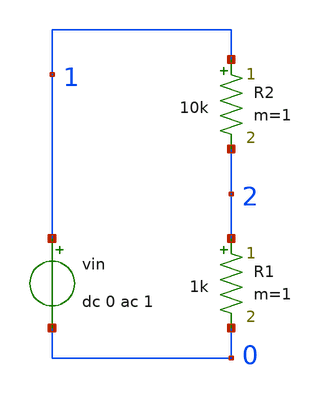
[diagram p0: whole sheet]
** sch_path: test_noise.sch
**.subckt test_noise
R1 2 0 1k m=1
R2 1 2 10k m=1
vin 1 0 dc 0 ac 1
**** begin user architecture code



.control
noise v(2,0) vin dec 100 1 1k
setplot noise1
plot inoise_spectrum onoise_spectrum
.endc


**** end user architecture code
**.ends
.end
